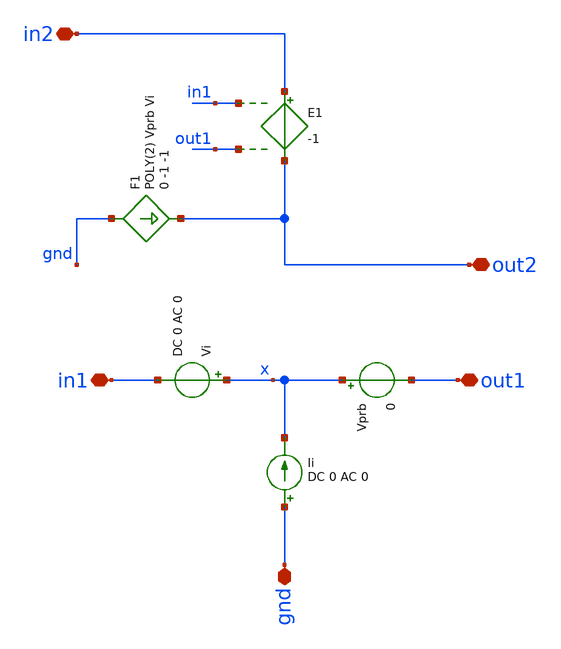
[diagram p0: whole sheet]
** sch_path: modules/cmdmprobe.sch
**.subckt cmdmprobe gnd in1 out1 in2 out2
*.iopin gnd
*.iopin in1
*.iopin out1
*.iopin in2
*.iopin out2
Ii gnd x DC 0 AC 0
Vi x in1 DC 0 AC 0
Vprb x out1 0
E1 in2 out2 in1 out1 -1
F1 gnd out2 POLY(2) Vprb Vi 0 -1 -1
**.ends
.end
